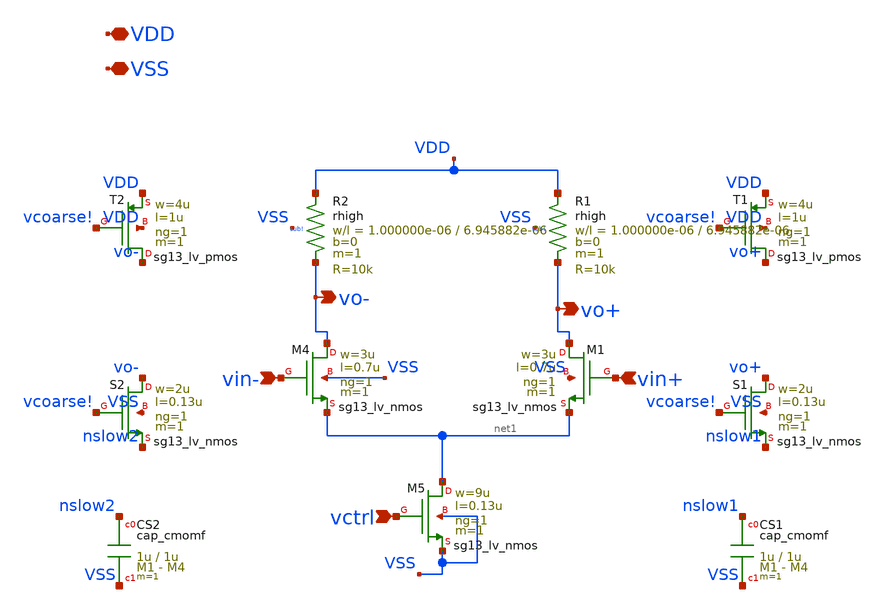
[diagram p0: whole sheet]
** sch_path: xschem/ring_inverter.sch
**.subckt ring_inverter VDD VSS vo+ vin- vctrl vo- vin+
*.iopin VDD
*.iopin VSS
*.opin vo+
*.ipin vin-
*.ipin vctrl
*.opin vo-
*.ipin vin+
XM4 vo- vin- net1 VSS sg13_lv_nmos w=3u l=0.7u ng=1 m=1 mm_ok=1
XM5 net1 vctrl VSS VSS sg13_lv_nmos w=9u l=0.13u ng=1 m=1 mm_ok=1
XM1 vo+ vin+ net1 VSS sg13_lv_nmos w=3u l=0.7u ng=1 m=1 mm_ok=1
XR1 VDD vo+ sub! rhigh w=1.000000e-06 l=6.945882e-06 m=1 b=0 mm_ok=1
XR2 VDD vo- sub! rhigh w=1.000000e-06 l=6.945882e-06 m=1 b=0 mm_ok=1
XT1 vo+ vcoarse! VDD VDD sg13_lv_pmos w=4u l=1u ng=1 m=1 mm_ok=1
XT2 vo- vcoarse! VDD VDD sg13_lv_pmos w=4u l=1u ng=1 m=1 mm_ok=1
XS1 vo+ vcoarse! nslow1 VSS sg13_lv_nmos w=2u l=0.13u ng=1 m=1 mm_ok=1
XCS1 nslow1 VSS cap_cmomf w=1u l=1u mmin=1 mmax=4 subblock=0 rfmodel=0 subscale=1 m=1 mm_ok=1
XS2 vo- vcoarse! nslow2 VSS sg13_lv_nmos w=2u l=0.13u ng=1 m=1 mm_ok=1
XCS2 nslow2 VSS cap_cmomf w=1u l=1u mmin=1 mmax=4 subblock=0 rfmodel=0 subscale=1 m=1 mm_ok=1
**.ends
.end
